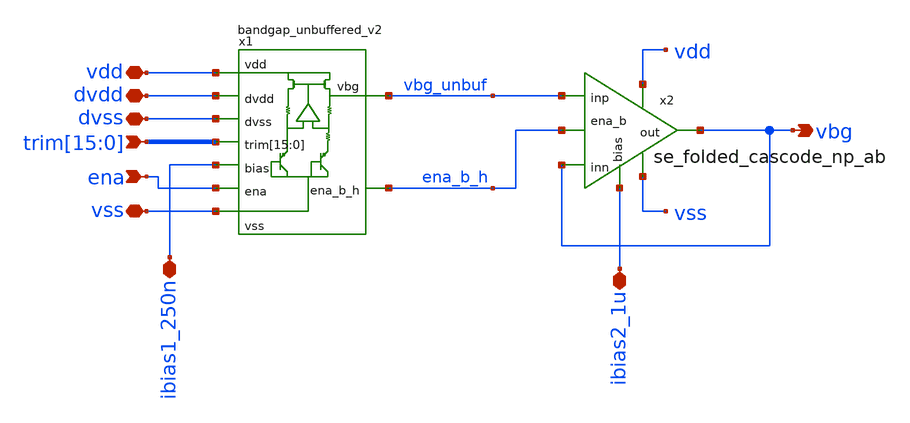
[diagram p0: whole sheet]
** sch_path: xschem/sg13cmos5l_ocd_ip__bandgap_v2.sch
**.subckt sg13cmos5l_ocd_ip__bandgap_v2
*+ trim[15],trim[14],trim[13],trim[12],trim[11],trim[10],trim[9],trim[8],trim[7],trim[6],trim[5],trim[4],trim[3],trim[2],trim[1],trim[0] ena vbg ibias2_1u ibias1_250n vdd dvdd dvss vss
*.ipin
*+ trim[15],trim[14],trim[13],trim[12],trim[11],trim[10],trim[9],trim[8],trim[7],trim[6],trim[5],trim[4],trim[3],trim[2],trim[1],trim[0]
*.ipin ena
*.opin vbg
*.iopin ibias2_1u
*.iopin ibias1_250n
*.iopin vdd
*.iopin dvdd
*.iopin dvss
*.iopin vss
x1 vdd vbg_unbuf vss ibias1_250n trim[15] trim[14] trim[13] trim[12] trim[11] trim[10] trim[9]
+ trim[8] trim[7] trim[6] trim[5] trim[4] trim[3] trim[2] trim[1] trim[0] dvss dvdd ena ena_b_h
+ bandgap_unbuffered_v2
x2 vdd vbg vbg_unbuf vbg vss ibias2_1u ena_b_h se_folded_cascode_np_ab
**.ends
.end
